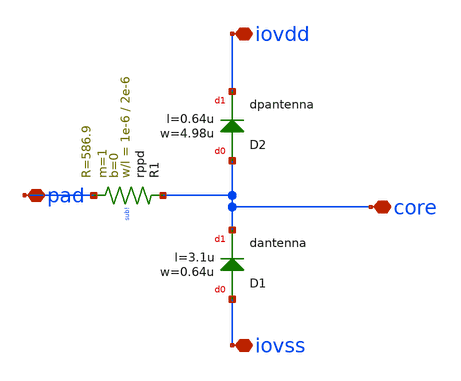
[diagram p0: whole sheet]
** sch_path: ihp-sg13g2/libs.ref/sg13g2_io/xschem/sg13g2_SecondaryProtection.sch
**.subckt sg13g2_SecondaryProtection iovdd iovss core pad
*.iopin iovdd
*.iopin iovss
*.iopin core
*.iopin pad
XR1 core pad sub! rppd w=1e-6 l=2e-6 m=1 b=0 mm_ok=1
XD1 iovss core dantenna l=3.1u w=0.64u
XD2 core iovdd dpantenna l=0.64u w=4.98u
**.ends
.end
